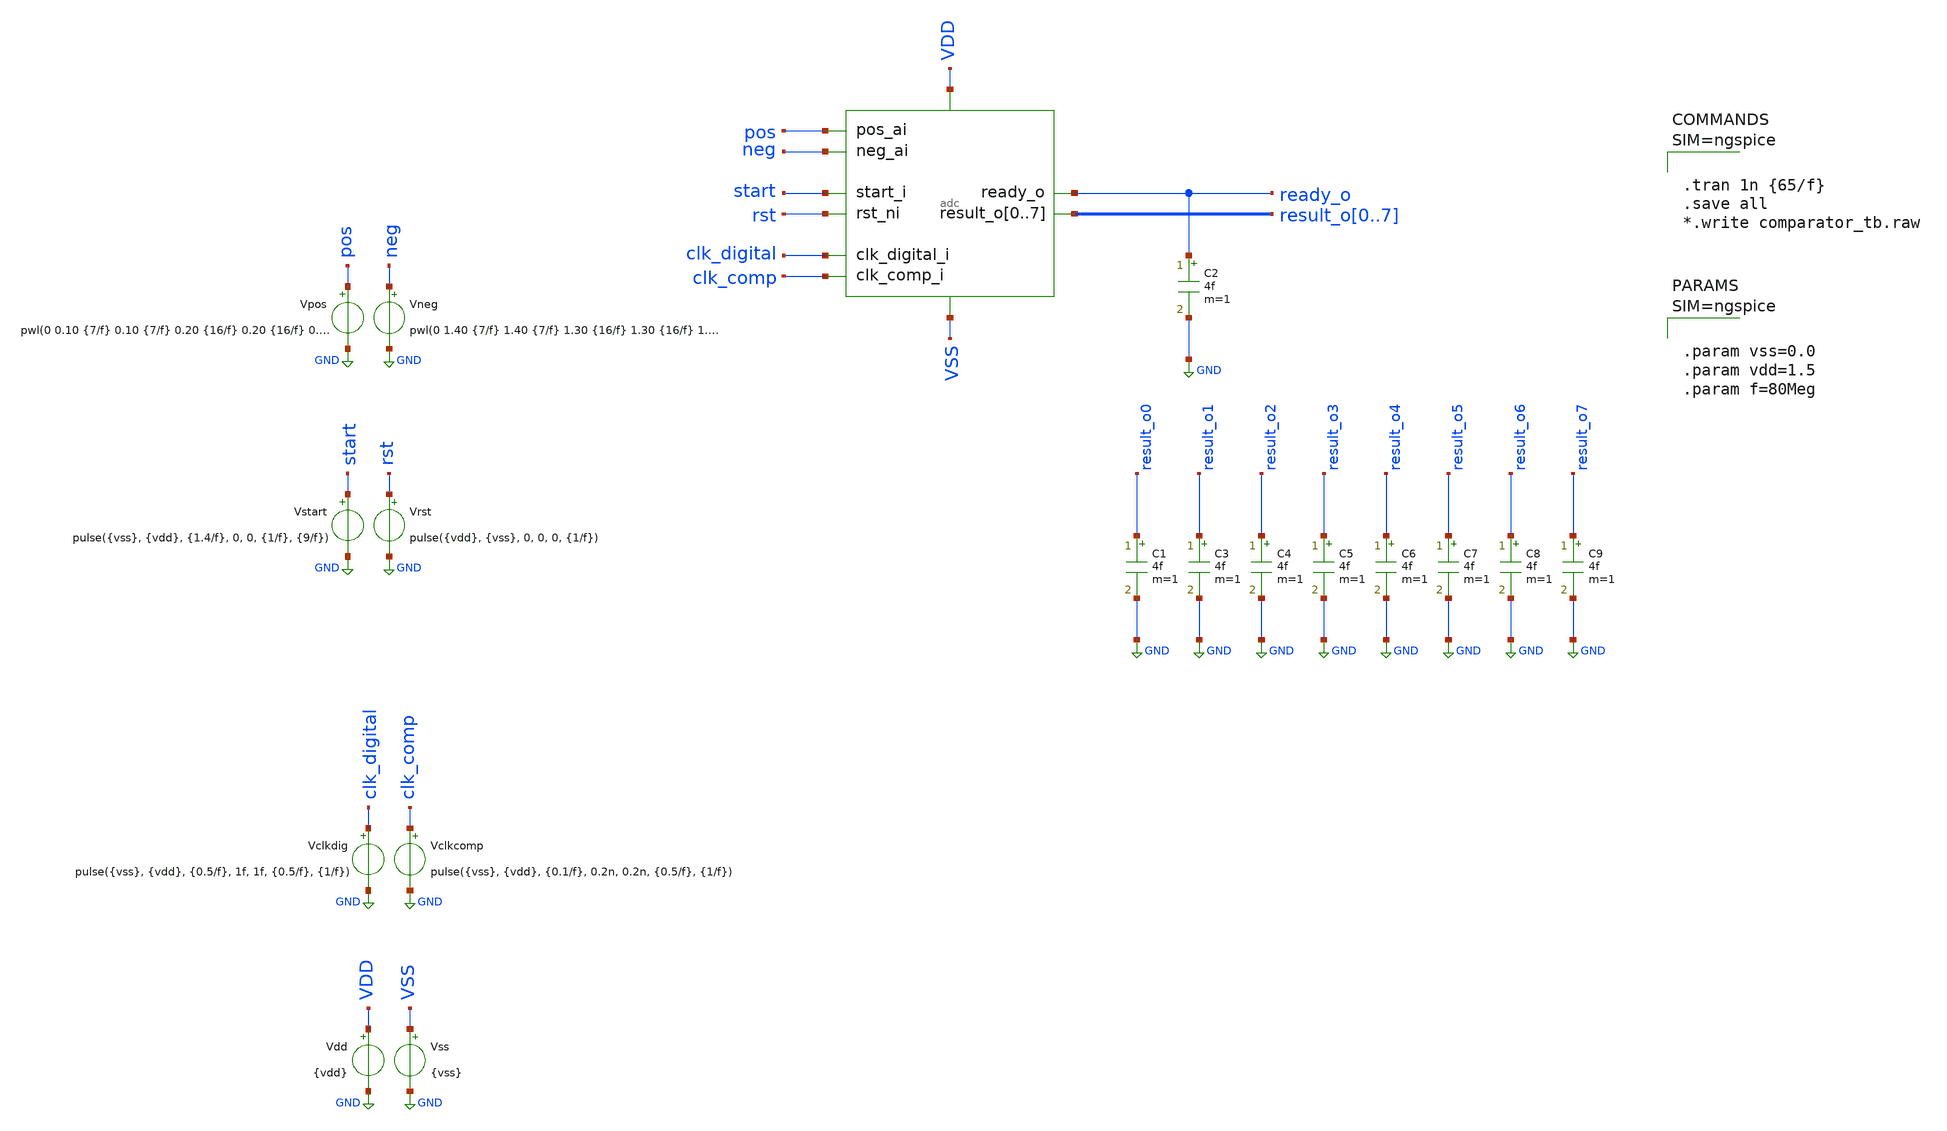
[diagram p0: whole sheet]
** sch_path: designs/diff_9cycle/xschem/adc_tb.sch
**.subckt adc_tb
x1 pos start rst clk_digital result_o0 result_o1 result_o2 result_o3 result_o4 result_o5 result_o6
+ result_o7 ready_o VDD VSS clk_comp neg adc
Vclkdig clk_digital GND pulse({vss}, {vdd}, {0.5/f}, 1f, 1f, {0.5/f}, {1/f})
Vrst rst GND pulse({vdd}, {vss}, 0, 0, 0, {1/f})
Vstart start GND pulse({vss}, {vdd}, {1.4/f}, 0, 0, {1/f}, {9/f})
Vpos pos GND pwl(0 0.10 {7/f} 0.10 {7/f} 0.20 {16/f} 0.20 {16/f} 0.30 {25/f} 0.30 {25/f} 0.40 {34/f}
+ 0.40 {34/f} 0.50 {43/f} 0.50 {43/f} 0.60 {52/f} 0.60 {52/f} 0.70 {61/f} 0.70 {61/f} 0.80 {70/f} 0.80
+ {70/f} 0.90 {79/f} 0.90 {79/f} 1.00 {88/f} 1.00 {88/f} 1.10 {97/f} 1.10 {97/f} 1.20 {106/f} 1.20 {106/f}
+ 1.30 {115/f} 1.30 {115/f} 1.40 {124/f} 1.40)
.save i(vpos)
Vdd VDD GND {vdd}
Vss VSS GND {vss}
C1 result_o0 GND 4f m=1
C2 ready_o GND 4f m=1
C3 result_o1 GND 4f m=1
C4 result_o2 GND 4f m=1
C5 result_o3 GND 4f m=1
Vclkcomp clk_comp GND pulse({vss}, {vdd}, {0.1/f}, 0.2n, 0.2n, {0.5/f}, {1/f})
C6 result_o4 GND 4f m=1
C7 result_o5 GND 4f m=1
C8 result_o6 GND 4f m=1
C9 result_o7 GND 4f m=1
Vneg neg GND pwl(0 1.40 {7/f} 1.40 {7/f} 1.30 {16/f} 1.30 {16/f} 1.20 {25/f} 1.20 {25/f} 1.10 {34/f}
+ 1.10 {34/f} 1.00 {43/f} 1.00 {43/f} 0.90 {52/f} 0.90 {52/f} 0.80 {61/f} 0.80 {61/f} 0.70 {70/f} 0.70
+ {70/f} 0.60 {79/f} 0.60 {79/f} 0.50 {88/f} 0.50 {88/f} 0.40 {97/f} 0.40 {97/f} 0.30 {106/f} 0.30 {106/f}
+ 0.20 {115/f} 0.20 {115/f} 0.10 {124/f} 0.10)
.save i(vneg)
**** begin user architecture code

.lib $::SG13G2_MODELS/cornerMOSlv.lib mos_tt
.lib $::SG13G2_MODELS/cornerCAP.lib cap_typ
.include $::PDK_ROOT/ihp-sg13g2/libs.ref/sg13g2_stdcell/spice/sg13g2_stdcell.spice




.tran 1n {65/f}
.save all
*.write comparator_tb.raw






.param vss=0.0
.param vdd=1.5
.param f=80Meg






.control
pre_set auto_bridge_d_out =  ( ".model auto_bridge_out bidi_bridge(direction=0 out_high=1.5
+ t_rise=0.2n t_fall=0.2n)"    "auto_bridge_out%d [ %s ] [ %s ] null auto_bridge_out" )
pre_set auto_bridge_d_in =  ( ".model auto_bridge_in bidi_bridge(direction=1 in_low=0.5 in_high=1)"
+    "auto_bridge_in%d [ %s ] [ %s ] null auto_bridge_in" )
.endc



**** end user architecture code
**.ends
.GLOBAL GND
.end
